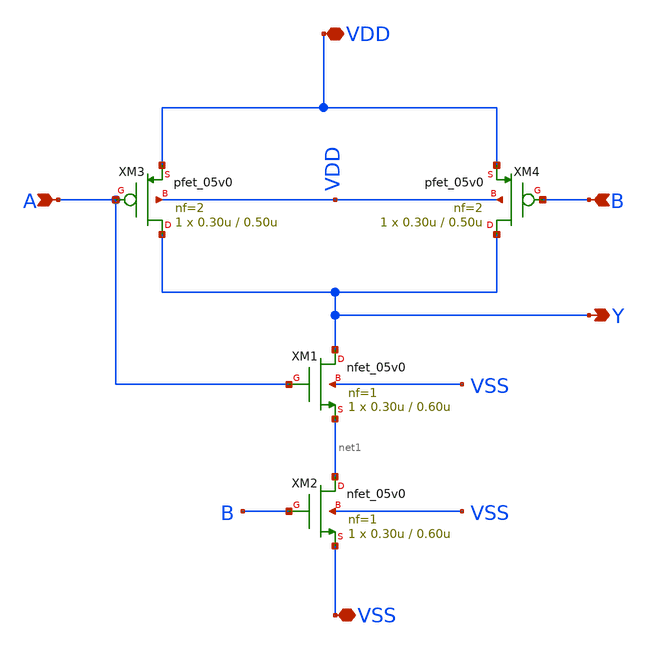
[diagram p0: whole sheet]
** sch_path: designs/libs/core_test/test_nand/test_nand.sch
**.subckt test_nand VDD VSS A B Y
*.iopin VDD
*.iopin VSS
*.ipin A
*.ipin B
*.opin Y
XM1 Y A net1 VSS nfet_05v0 L=0.60u W=0.30u nf=1 ad='int((nf+1)/2) * W/nf * 0.18u' as='int((nf+2)/2) * W/nf * 0.18u'
+ pd='2*int((nf+1)/2) * (W/nf + 0.18u)' ps='2*int((nf+2)/2) * (W/nf + 0.18u)' nrd='0.18u / W' nrs='0.18u / W'
+ sa=0 sb=0 sd=0 m=1
XM2 net1 B VSS VSS nfet_05v0 L=0.60u W=0.30u nf=1 ad='int((nf+1)/2) * W/nf * 0.18u' as='int((nf+2)/2) * W/nf * 0.18u'
+ pd='2*int((nf+1)/2) * (W/nf + 0.18u)' ps='2*int((nf+2)/2) * (W/nf + 0.18u)' nrd='0.18u / W' nrs='0.18u / W'
+ sa=0 sb=0 sd=0 m=1
XM3 Y A VDD VDD pfet_05v0 L=0.50u W=0.30u nf=2 ad='int((nf+1)/2) * W/nf * 0.18u' as='int((nf+2)/2) * W/nf * 0.18u'
+ pd='2*int((nf+1)/2) * (W/nf + 0.18u)' ps='2*int((nf+2)/2) * (W/nf + 0.18u)' nrd='0.18u / W' nrs='0.18u / W'
+ sa=0 sb=0 sd=0 m=1
XM4 Y B VDD VDD pfet_05v0 L=0.50u W=0.30u nf=2 ad='int((nf+1)/2) * W/nf * 0.18u' as='int((nf+2)/2) * W/nf * 0.18u'
+ pd='2*int((nf+1)/2) * (W/nf + 0.18u)' ps='2*int((nf+2)/2) * (W/nf + 0.18u)' nrd='0.18u / W' nrs='0.18u / W'
+ sa=0 sb=0 sd=0 m=1
**.ends
.end
